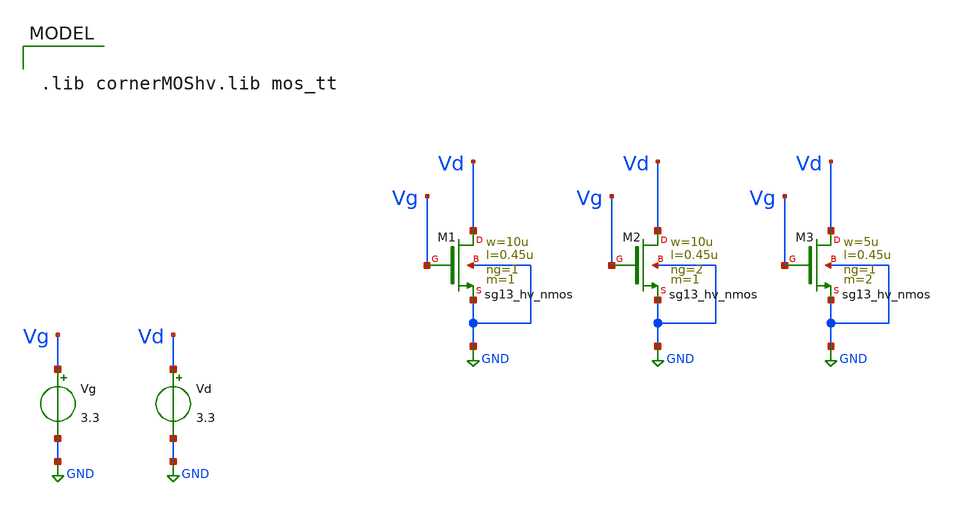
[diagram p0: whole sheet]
** sch_path: xschem/CMOS_Char/Vds_HvMOS.sch
**.subckt Vds_HvMOS
XM1 Vd Vg GND GND sg13_hv_nmos w=10u l=0.45u ng=1 m=1 mm_ok=1
XM2 Vd Vg GND GND sg13_hv_nmos w=10u l=0.45u ng=2 m=1 mm_ok=1
XM3 Vd Vg GND GND sg13_hv_nmos w=5u l=0.45u ng=1 m=2 mm_ok=1
Vg Vg GND 3.3
Vd Vd GND 3.3
**** begin user architecture code



.control

*** ALMACENAR DATOS Y CORRER SIMULACION

save all  @n.xm1.nsg13_hv_nmos[vds]  @n.xm1.nsg13_hv_nmos[ids]  @n.xm1.nsg13_hv_nmos[gds]
+  @n.xm1.nsg13_hv_nmos[weff]  @n.xm2.nsg13_hv_nmos[vds]  @n.xm2.nsg13_hv_nmos[ids]  @n.xm2.nsg13_hv_nmos[gds]
+  @n.xm2.nsg13_hv_nmos[weff]  @n.xm3.nsg13_hv_nmos[vds]  @n.xm3.nsg13_hv_nmos[ids]  @n.xm3.nsg13_hv_nmos[gds]
+  @n.xm3.nsg13_hv_nmos[weff]

dc Vd 0 3.3 0.01 Vg 1.32 3.3 0.66

*** GUARDAR DATOS COMO VARIABLES Y GRAFICAR

let vds1 = @n.xm1.nsg13_hv_nmos[vds]
let ids1 = @n.xm1.nsg13_hv_nmos[ids]
let vds2 = @n.xm2.nsg13_hv_nmos[vds]
let ids2 = @n.xm2.nsg13_hv_nmos[ids]

let vds3 = @n.xm3.nsg13_hv_nmos[vds]
let ids3 = @n.xm3.nsg13_hv_nmos[ids]
let rds3 = 1/@n.xm3.nsg13_hv_nmos[gds]

plot rds3 vs vds3
plot ids1 vs vds1
plot ids2 vs vds2
plot ids3 vs vds3

op
let ids1 = @n.xm1.nsg13_hv_nmos[ids]
let ids2 = @n.xm2.nsg13_hv_nmos[ids]
let ids3 = @n.xm3.nsg13_hv_nmos[ids]

let weff1 = @n.xm1.nsg13_hv_nmos[weff]
let weff2 = @n.xm2.nsg13_hv_nmos[weff]
let weff3 = @n.xm3.nsg13_hv_nmos[weff]
print weff1 weff2 weff3
.endc



.lib cornerMOShv.lib mos_tt

**** end user architecture code
**.ends
.GLOBAL GND
.end
